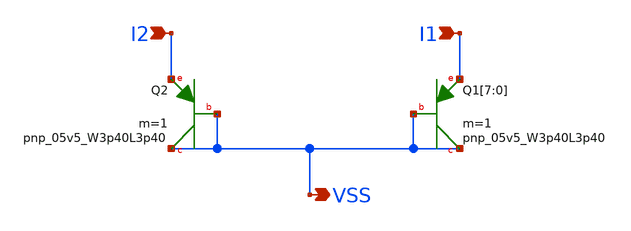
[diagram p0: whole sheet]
** sch_path: design/LELO_GR01_SKY130A/Diodes.sch
**.subckt Diodes VSS I2 I1
*.opin VSS
*.ipin I2
*.ipin I1
Q1[7] VSS pnp_05v5_W3p40L3p40
Q1[6] VSS pnp_05v5_W3p40L3p40
Q1[5] VSS pnp_05v5_W3p40L3p40
Q1[4] VSS pnp_05v5_W3p40L3p40
Q1[3] VSS pnp_05v5_W3p40L3p40
Q1[2] VSS pnp_05v5_W3p40L3p40
Q1[1] VSS pnp_05v5_W3p40L3p40
Q1[0] VSS pnp_05v5_W3p40L3p40
Q2 VSS pnp_05v5_W3p40L3p40
**.ends
.end
